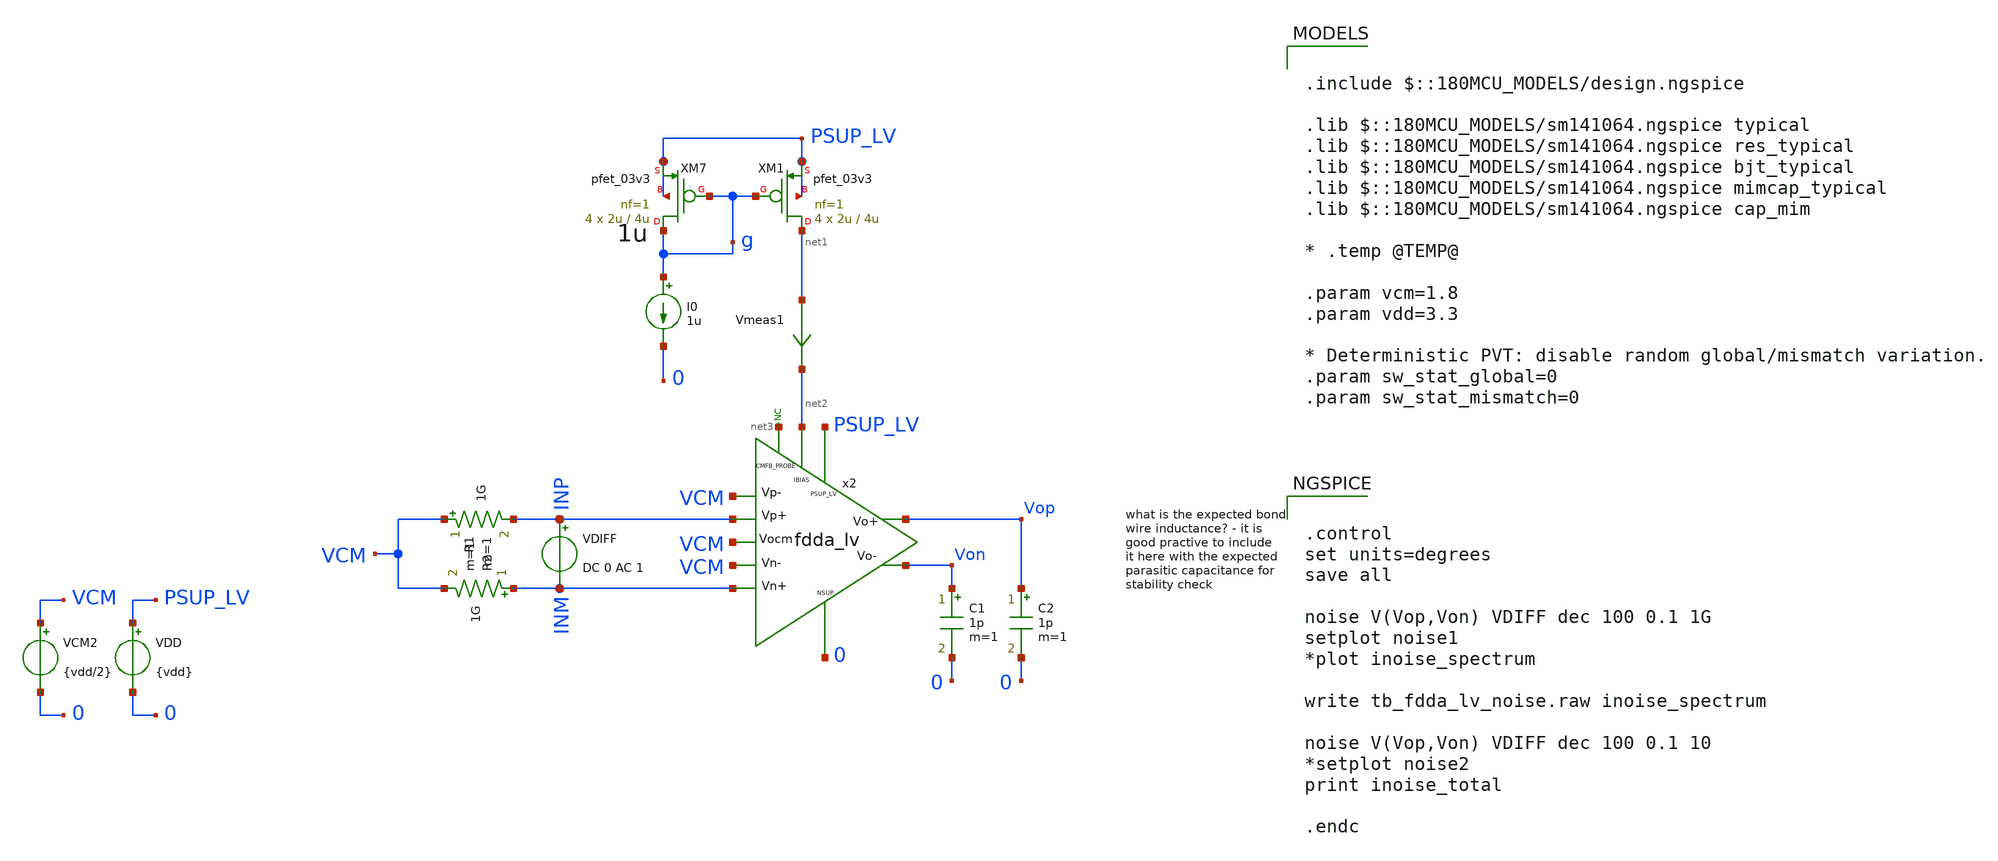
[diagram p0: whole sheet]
** sch_path: xschem/blocks/fdda_lv/tb_fdda_lv_noise.sch
**.subckt tb_fdda_lv_noise
C1 Von 0 1p m=1
x2 PSUP_LV VCM VCM INM INP Vop Von net2 0 net3 VCM fdda_lv
VDD PSUP_LV 0 {vdd}
C2 Vop 0 1p m=1
VCM2 VCM 0 {vdd/2}
VDIFF INP INM DC 0 AC 1
R1 VCM INP 1G m=1
R2 INM VCM 1G m=1
XM7 g g PSUP_LV PSUP_LV pfet_03v3 L=4u W=2u nf=1 ad='int((nf+1)/2) * W/nf * 0.18u' as='int((nf+2)/2) * W/nf * 0.18u'
+ pd='2*int((nf+1)/2) * (W/nf + 0.18u)' ps='2*int((nf+2)/2) * (W/nf + 0.18u)' nrd='0.18u / W' nrs='0.18u / W'
+ sa=0 sb=0 sd=0 m=4
XM1 net1 g PSUP_LV PSUP_LV pfet_03v3 L=4u W=2u nf=1 ad='int((nf+1)/2) * W/nf * 0.18u' as='int((nf+2)/2) * W/nf * 0.18u'
+ pd='2*int((nf+1)/2) * (W/nf + 0.18u)' ps='2*int((nf+2)/2) * (W/nf + 0.18u)' nrd='0.18u / W' nrs='0.18u / W'
+ sa=0 sb=0 sd=0 m=4
I0 g 0 1u
Vmeas1 net1 net2 0
.save i(vmeas1)
* noconn #net3
**** begin user architecture code

.include $::180MCU_MODELS/design.ngspice

.lib $::180MCU_MODELS/sm141064.ngspice typical
.lib $::180MCU_MODELS/sm141064.ngspice res_typical
.lib $::180MCU_MODELS/sm141064.ngspice bjt_typical
.lib $::180MCU_MODELS/sm141064.ngspice mimcap_typical
.lib $::180MCU_MODELS/sm141064.ngspice cap_mim

* .temp @TEMP@

.param vcm=1.8
.param vdd=3.3

* Deterministic PVT: disable random global/mismatch variation.
.param sw_stat_global=0
.param sw_stat_mismatch=0



.control
set units=degrees
save all

noise V(Vop,Von) VDIFF dec 100 0.1 1G
setplot noise1
*plot inoise_spectrum

write tb_fdda_lv_noise.raw inoise_spectrum

noise V(Vop,Von) VDIFF dec 100 0.1 10
*setplot noise2
print inoise_total

.endc


**** end user architecture code
**.ends
.end
